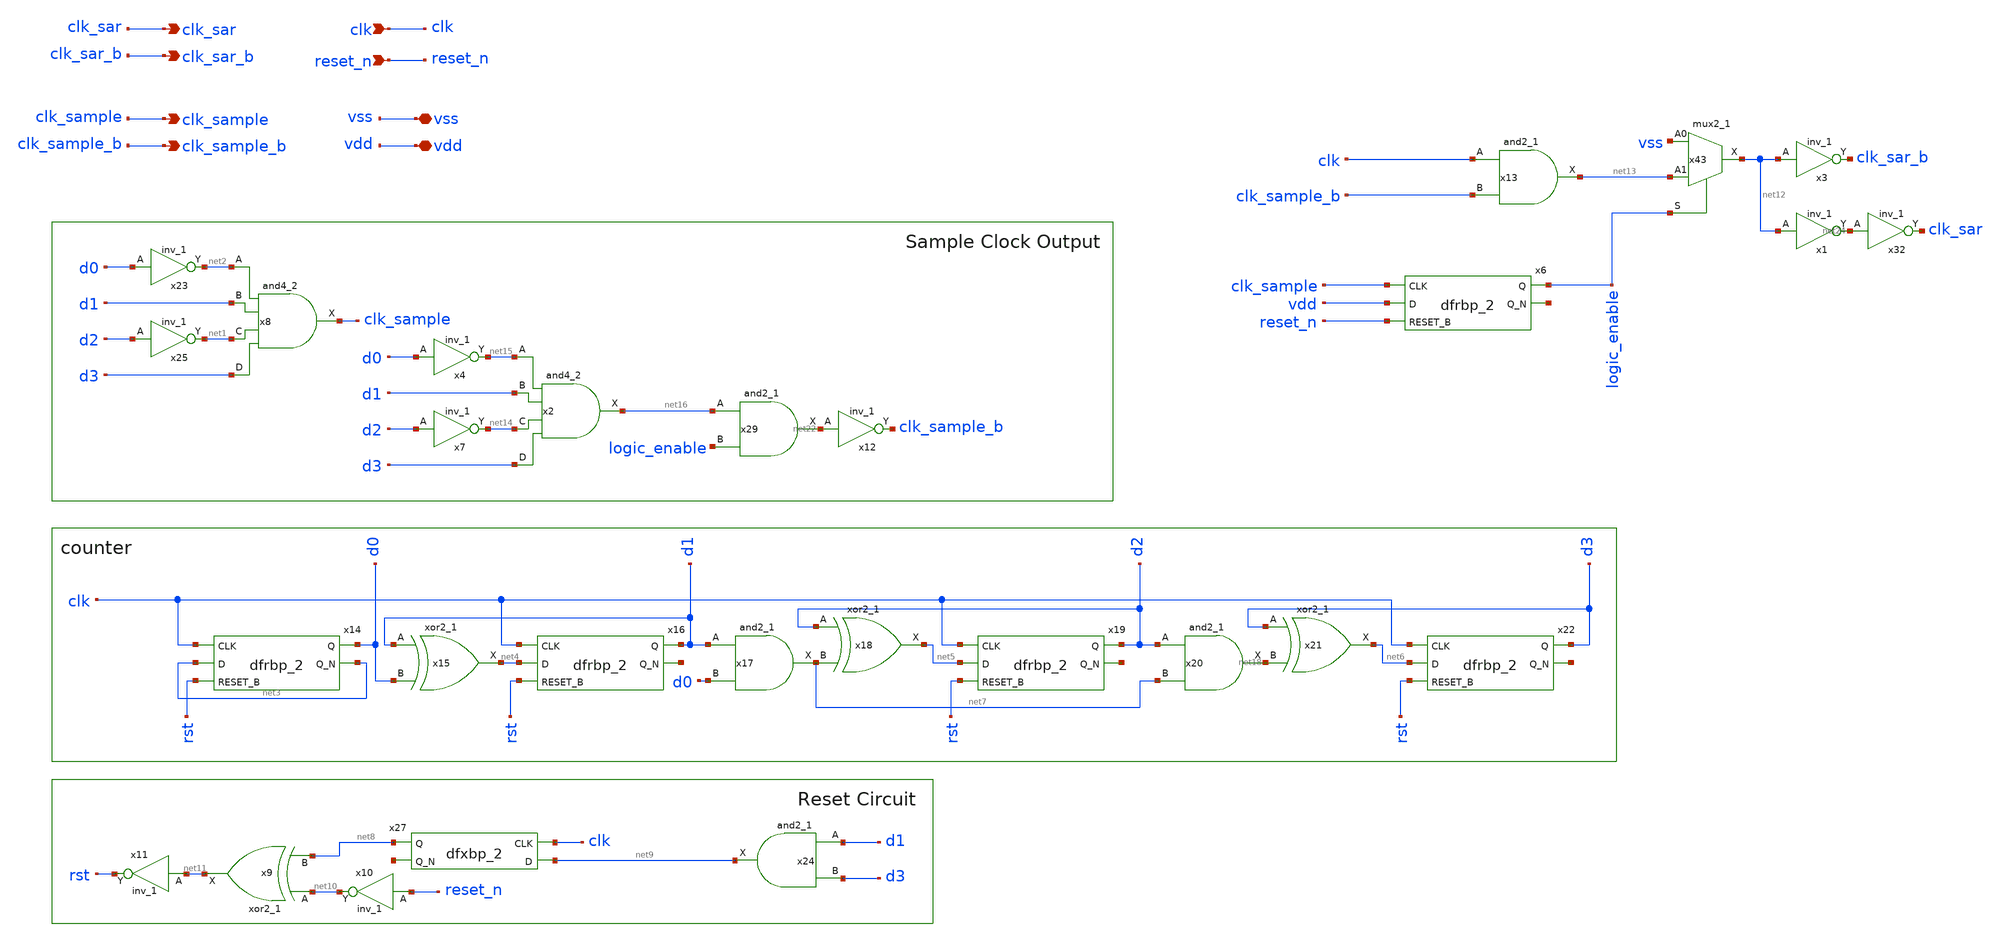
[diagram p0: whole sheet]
** sch_path: xschem/clockgen/clockgen.sch
**.subckt clockgen clk_sar clk_sample clk vss vdd clk_sar_b clk_sample_b reset_n
*.opin clk_sar
*.opin clk_sample
*.ipin clk
*.iopin vss
*.iopin vdd
*.opin clk_sar_b
*.opin clk_sample_b
*.ipin reset_n
x8 net2 d1 net1 d3 vss vss vdd vdd clk_sample sky130_fd_sc_hd__and4_2
x14 clk net3 rst vss vss vdd vdd d0 net3 sky130_fd_sc_hd__dfrbp_2
x15 d1 d0 vss vss vdd vdd net4 sky130_fd_sc_hd__xor2_1
x16 clk net4 rst vss vss vdd vdd d1 net17 sky130_fd_sc_hd__dfrbp_2
x17 d1 d0 vss vss vdd vdd net7 sky130_fd_sc_hd__and2_1
x18 d2 net7 vss vss vdd vdd net5 sky130_fd_sc_hd__xor2_1
x20 d2 net7 vss vss vdd vdd net18 sky130_fd_sc_hd__and2_1
x21 d3 net18 vss vss vdd vdd net6 sky130_fd_sc_hd__xor2_1
x19 clk net5 rst vss vss vdd vdd d2 net19 sky130_fd_sc_hd__dfrbp_2
x22 clk net6 rst vss vss vdd vdd d3 net20 sky130_fd_sc_hd__dfrbp_2
x23 d0 vss vss vdd vdd net2 sky130_fd_sc_hd__inv_1
x25 d2 vss vss vdd vdd net1 sky130_fd_sc_hd__inv_1
x24 d1 d3 vss vss vdd vdd net9 sky130_fd_sc_hd__and2_1
x27 clk net9 vss vss vdd vdd net8 net21 sky130_fd_sc_hd__dfxbp_2
x9 net10 net8 vss vss vdd vdd net11 sky130_fd_sc_hd__xor2_1
x10 reset_n vss vss vdd vdd net10 sky130_fd_sc_hd__inv_1
x11 net11 vss vss vdd vdd rst sky130_fd_sc_hd__inv_1
x12 net22 vss vss vdd vdd clk_sample_b sky130_fd_sc_hd__inv_1
x6 clk_sample vdd reset_n vss vss vdd vdd logic_enable net23 sky130_fd_sc_hd__dfrbp_2
x43 vss net13 logic_enable vss vss vdd vdd net12 sky130_fd_sc_hd__mux2_1
x13 clk clk_sample_b vss vss vdd vdd net13 sky130_fd_sc_hd__and2_1
x1 net12 vss vss vdd vdd net24 sky130_fd_sc_hd__inv_1
x3 net12 vss vss vdd vdd clk_sar_b sky130_fd_sc_hd__inv_1
x32 net24 vss vss vdd vdd clk_sar sky130_fd_sc_hd__inv_1
x29 net16 logic_enable vss vss vdd vdd net22 sky130_fd_sc_hd__and2_1
x2 net15 d1 net14 d3 vss vss vdd vdd net16 sky130_fd_sc_hd__and4_2
x4 d0 vss vss vdd vdd net15 sky130_fd_sc_hd__inv_1
x7 d2 vss vss vdd vdd net14 sky130_fd_sc_hd__inv_1
**.ends
.end
